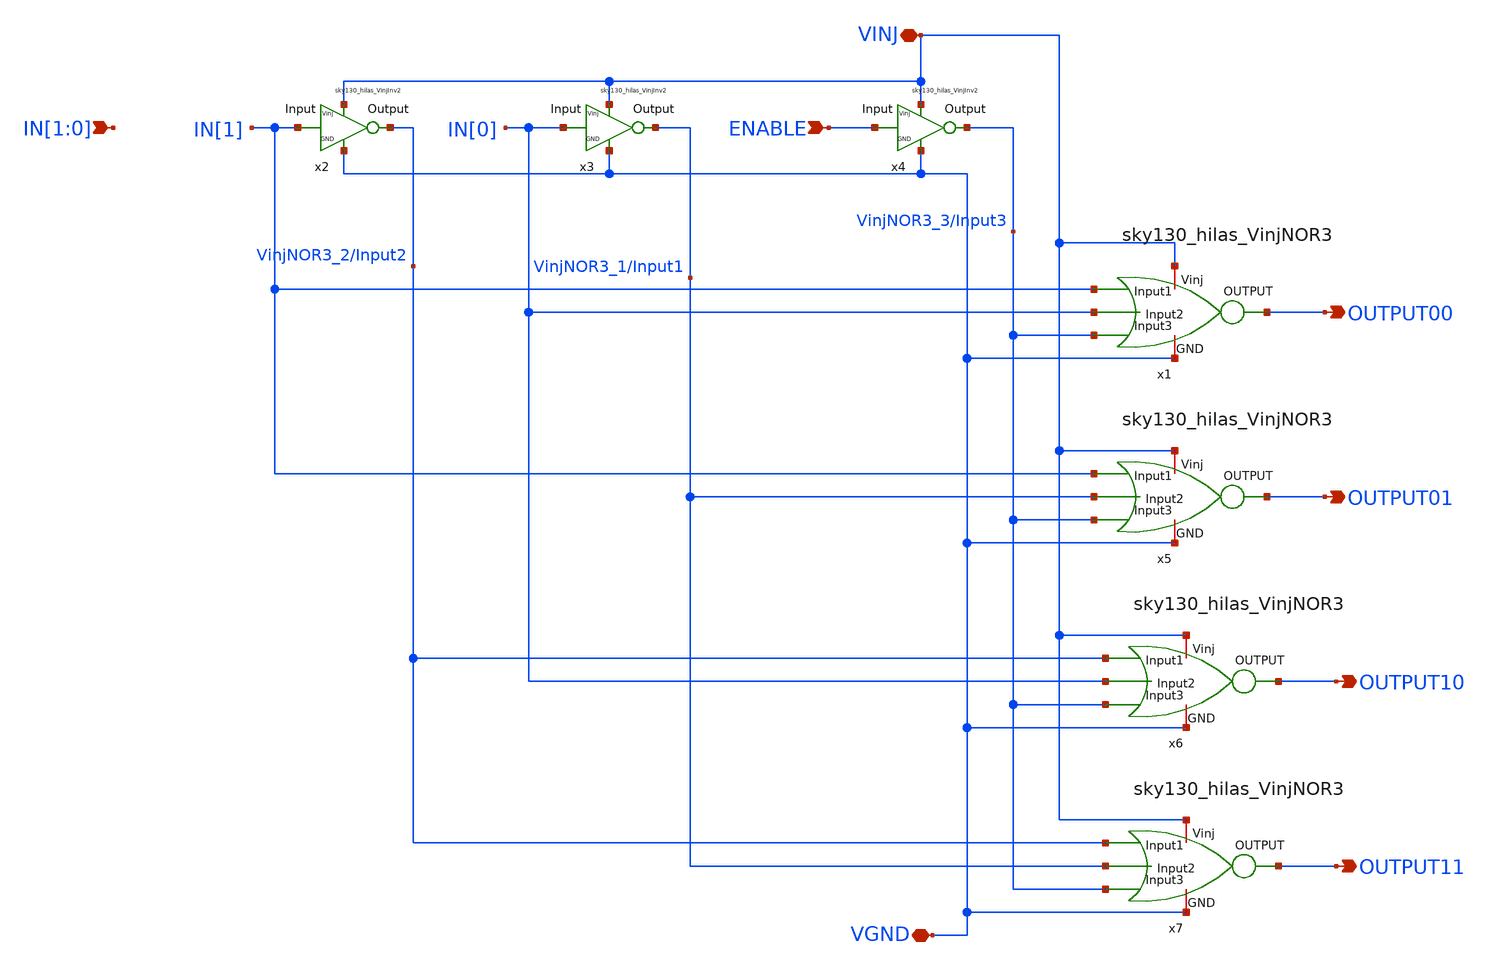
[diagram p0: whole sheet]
** sch_path: sky130_cells/RDAC/Design/sky130_hilas_VinjDecode2to4.sch
**.subckt sky130_hilas_VinjDecode2to4 ENABLE OUTPUT00 OUTPUT01 OUTPUT10 OUTPUT11 VINJ VGND
*+ IN[1],IN[0]
*.ipin ENABLE
*.opin OUTPUT00
*.opin OUTPUT01
*.opin OUTPUT10
*.opin OUTPUT11
*.iopin VINJ
*.iopin VGND
*.ipin IN[1],IN[0]
x2 VINJ IN[1] VinjNOR3_2/Input2 VGND sky130_hilas_VinjInv2
x3 VINJ IN[0] VinjNOR3_1/Input1 VGND sky130_hilas_VinjInv2
x4 VINJ ENABLE VinjNOR3_3/Input3 VGND sky130_hilas_VinjInv2
x1 VINJ IN[1] IN[0] VinjNOR3_3/Input3 OUTPUT00 VGND sky130_hilas_VinjNOR3
x5 VINJ IN[1] VinjNOR3_1/Input1 VinjNOR3_3/Input3 OUTPUT01 VGND sky130_hilas_VinjNOR3
x6 VINJ VinjNOR3_2/Input2 IN[0] VinjNOR3_3/Input3 OUTPUT10 VGND sky130_hilas_VinjNOR3
x7 VINJ VinjNOR3_2/Input2 VinjNOR3_1/Input1 VinjNOR3_3/Input3 OUTPUT11 VGND sky130_hilas_VinjNOR3
**.ends

* expanding   symbol:  sky130_cells/RDAC/Design/sky130_hilas_VinjInv2.sym # of pins=4
** sym_path: sky130_cells/RDAC/Design/sky130_hilas_VinjInv2.sym
** sch_path: sky130_cells/RDAC/Design/sky130_hilas_VinjInv2.sch
.subckt sky130_hilas_VinjInv2 Vinj Input Output GND
*.ipin Input
*.opin Output
*.iopin Vinj
*.iopin GND
XM4 Output Input Vinj Vinj sky130_fd_pr__pfet_g5v0d10v5 L=0.53 W=0.42 nf=1 ad='int((nf+1)/2) * W/nf * 0.29'
+ as='int((nf+2)/2) * W/nf * 0.29' pd='2*int((nf+1)/2) * (W/nf + 0.29)' ps='2*int((nf+2)/2) * (W/nf + 0.29)'
+ nrd='0.29 / W' nrs='0.29 / W' sa=0 sb=0 sd=0 mult=1 m=1
XM3 Output Input GND GND sky130_fd_pr__nfet_g5v0d10v5 L=0.52 W=0.42 nf=1 ad='int((nf+1)/2) * W/nf * 0.29'
+ as='int((nf+2)/2) * W/nf * 0.29' pd='2*int((nf+1)/2) * (W/nf + 0.29)' ps='2*int((nf+2)/2) * (W/nf + 0.29)'
+ nrd='0.29 / W' nrs='0.29 / W' sa=0 sb=0 sd=0 mult=1 m=1
.ends


* expanding   symbol:  sky130_cells/RDAC/Design/sky130_hilas_VinjNOR3.sym # of pins=6
** sym_path: sky130_cells/RDAC/Design/sky130_hilas_VinjNOR3.sym
** sch_path: sky130_cells/RDAC/Design/sky130_hilas_VinjNOR3.sch
.subckt sky130_hilas_VinjNOR3 Vinj Input1 Input2 Input3 OUTPUT GND
*.ipin Input3
*.ipin Input1
*.ipin Input2
*.iopin Vinj
*.iopin GND
*.opin OUTPUT
XM1 OUTPUT Input3 GND GND sky130_fd_pr__nfet_g5v0d10v5 L=0.5 W=0.42 nf=1 ad='int((nf+1)/2) * W/nf * 0.29'
+ as='int((nf+2)/2) * W/nf * 0.29' pd='2*int((nf+1)/2) * (W/nf + 0.29)' ps='2*int((nf+2)/2) * (W/nf + 0.29)'
+ nrd='0.29 / W' nrs='0.29 / W' sa=0 sb=0 sd=0 mult=1 m=1
XM2 OUTPUT Input1 GND GND sky130_fd_pr__nfet_g5v0d10v5 L=0.51 W=0.43 nf=1 ad='int((nf+1)/2) * W/nf * 0.29'
+ as='int((nf+2)/2) * W/nf * 0.29' pd='2*int((nf+1)/2) * (W/nf + 0.29)' ps='2*int((nf+2)/2) * (W/nf + 0.29)'
+ nrd='0.29 / W' nrs='0.29 / W' sa=0 sb=0 sd=0 mult=1 m=1
XM3 OUTPUT Input2 GND GND sky130_fd_pr__nfet_g5v0d10v5 L=0.5 W=0.42 nf=1 ad='int((nf+1)/2) * W/nf * 0.29'
+ as='int((nf+2)/2) * W/nf * 0.29' pd='2*int((nf+1)/2) * (W/nf + 0.29)' ps='2*int((nf+2)/2) * (W/nf + 0.29)'
+ nrd='0.29 / W' nrs='0.29 / W' sa=0 sb=0 sd=0 mult=1 m=1
XM6 OUTPUT Input2 net2 Vinj sky130_fd_pr__pfet_g5v0d10v5 L=0.52 W=0.43 nf=1 ad='int((nf+1)/2) * W/nf * 0.29'
+ as='int((nf+2)/2) * W/nf * 0.29' pd='2*int((nf+1)/2) * (W/nf + 0.29)' ps='2*int((nf+2)/2) * (W/nf + 0.29)'
+ nrd='0.29 / W' nrs='0.29 / W' sa=0 sb=0 sd=0 mult=1 m=1
XM4 net2 Input1 net1 Vinj sky130_fd_pr__pfet_g5v0d10v5 L=0.52 W=0.42 nf=1 ad='int((nf+1)/2) * W/nf * 0.29'
+ as='int((nf+2)/2) * W/nf * 0.29' pd='2*int((nf+1)/2) * (W/nf + 0.29)' ps='2*int((nf+2)/2) * (W/nf + 0.29)'
+ nrd='0.29 / W' nrs='0.29 / W' sa=0 sb=0 sd=0 mult=1 m=1
XM5 net1 Input3 Vinj Vinj sky130_fd_pr__pfet_g5v0d10v5 L=0.53 W=0.42 nf=1 ad='int((nf+1)/2) * W/nf * 0.29'
+ as='int((nf+2)/2) * W/nf * 0.29' pd='2*int((nf+1)/2) * (W/nf + 0.29)' ps='2*int((nf+2)/2) * (W/nf + 0.29)'
+ nrd='0.29 / W' nrs='0.29 / W' sa=0 sb=0 sd=0 mult=1 m=1
.ends

.end
